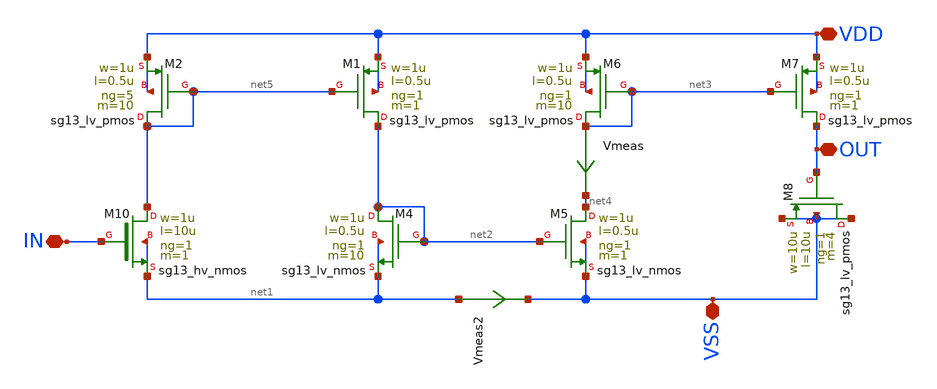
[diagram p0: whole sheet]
** sch_path: Delay_Circuit/Delay.sch
**.subckt Delay VDD OUT VSS IN
*.iopin VDD
*.iopin OUT
*.iopin VSS
*.iopin IN
XM4 net2 net2 net1 net1 sg13_lv_nmos w=1u l=0.5u ng=1 m=10 mm_ok=1
XM5 net4 net2 VSS VSS sg13_lv_nmos w=1u l=0.5u ng=1 m=1 mm_ok=1
XM6 net3 net3 VDD VDD sg13_lv_pmos w=1u l=0.5u ng=1 m=10 mm_ok=1
XM7 OUT net3 VDD VDD sg13_lv_pmos w=1u l=0.5u ng=1 m=1 mm_ok=1
XM8 VSS OUT VSS VSS sg13_lv_pmos w=10u l=10u ng=1 m=4 mm_ok=1
Vmeas net3 net4 0
.save i(vmeas)
Vmeas2 net1 VSS 0
.save i(vmeas2)
XM10 net5 IN net1 net1 sg13_hv_nmos w=1u l=10u ng=1 m=1 mm_ok=1
XM1 net2 net5 VDD VDD sg13_lv_pmos w=1u l=0.5u ng=1 m=1 mm_ok=1
XM2 net5 net5 VDD VDD sg13_lv_pmos w=1u l=0.5u ng=5 m=10 mm_ok=1
**.ends
.end
